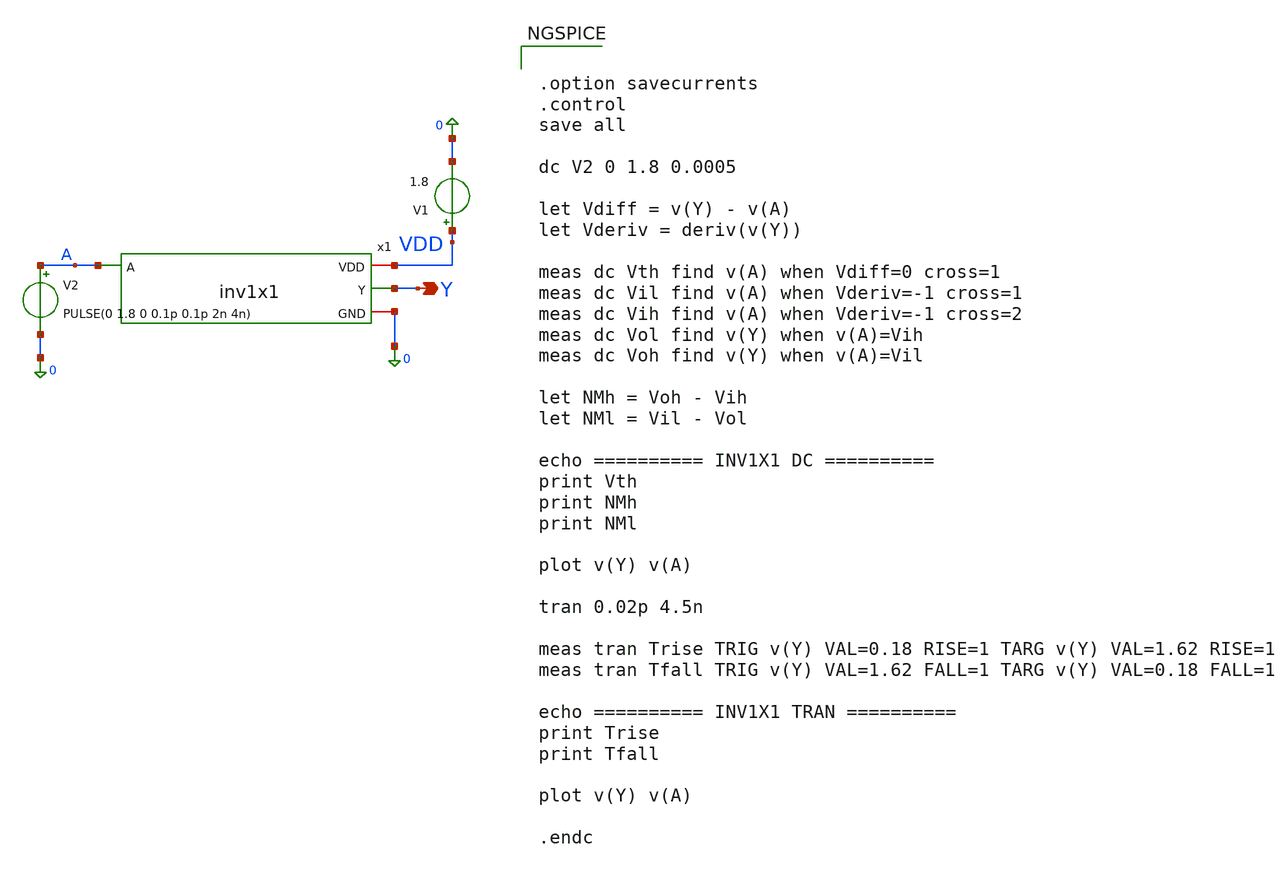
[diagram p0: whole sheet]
** sch_path: cells/INV1X1/schematic/inv1x1_tb.sch
**.subckt inv1x1_tb Y
*.opin Y
V2 A 0 PULSE(0 1.8 0 0.1p 0.1p 2n 4n)
V1 VDD 0 1.8
x1 VDD A Y 0 inv1x1
**** begin user architecture code

** opencircuitdesign pdks install
.lib $::SKYWATER_MODELS/sky130.lib.spice tt



.option savecurrents
.control
save all

dc V2 0 1.8 0.0005

let Vdiff = v(Y) - v(A)
let Vderiv = deriv(v(Y))

meas dc Vth find v(A) when Vdiff=0 cross=1
meas dc Vil find v(A) when Vderiv=-1 cross=1
meas dc Vih find v(A) when Vderiv=-1 cross=2
meas dc Vol find v(Y) when v(A)=Vih
meas dc Voh find v(Y) when v(A)=Vil

let NMh = Voh - Vih
let NMl = Vil - Vol

echo ========== INV1X1 DC ==========
print Vth
print NMh
print NMl

plot v(Y) v(A)

tran 0.02p 4.5n

meas tran Trise TRIG v(Y) VAL=0.18 RISE=1 TARG v(Y) VAL=1.62 RISE=1
meas tran Tfall TRIG v(Y) VAL=1.62 FALL=1 TARG v(Y) VAL=0.18 FALL=1

echo ========== INV1X1 TRAN ==========
print Trise
print Tfall

plot v(Y) v(A)

.endc


**** end user architecture code
**.ends

* expanding   symbol:  /foss/designs/SUB-VT_STD_CELL_LIB/cells/INV1X1/schematic/inv1x1.sym # of
*+ pins=4
** sym_path: cells/INV1X1/schematic/inv1x1.sym
** sch_path: cells/INV1X1/schematic/inv1x1.sch
.subckt inv1x1 VDD A Y GND
*.ipin A
*.opin Y
*.iopin VDD
*.iopin GND
XM1 Y A GND GND sky130_fd_pr__nfet_01v8 L=0.15 W=0.42 nf=1 ad='int((1 + 1)/2) * 0.42 / 1 * 0.29' as='int((1 + 2)/2) * 0.42 / 1 * 0.29'
+ pd='2*int((1 + 1)/2) * (0.42 / 1 + 0.29)' ps='2*int((1 + 2)/2) * (0.42 / 1 + 0.29)' nrd='0.29 / 0.42 '
+ nrs='0.29 / 0.42 ' sa=0 sb=0 sd=0 mult=1 m=1
XM2 Y A VDD VDD sky130_fd_pr__pfet_01v8 L=0.15 W=1.26 nf=1 ad='int((1 + 1)/2) * 1.26 / 1 * 0.29' as='int((1 + 2)/2) * 1.26 / 1 * 0.29'
+ pd='2*int((1 + 1)/2) * (1.26 / 1 + 0.29)' ps='2*int((1 + 2)/2) * (1.26 / 1 + 0.29)' nrd='0.29 / 1.26 '
+ nrs='0.29 / 1.26 ' sa=0 sb=0 sd=0 mult=1 m=1
.ends

.end
